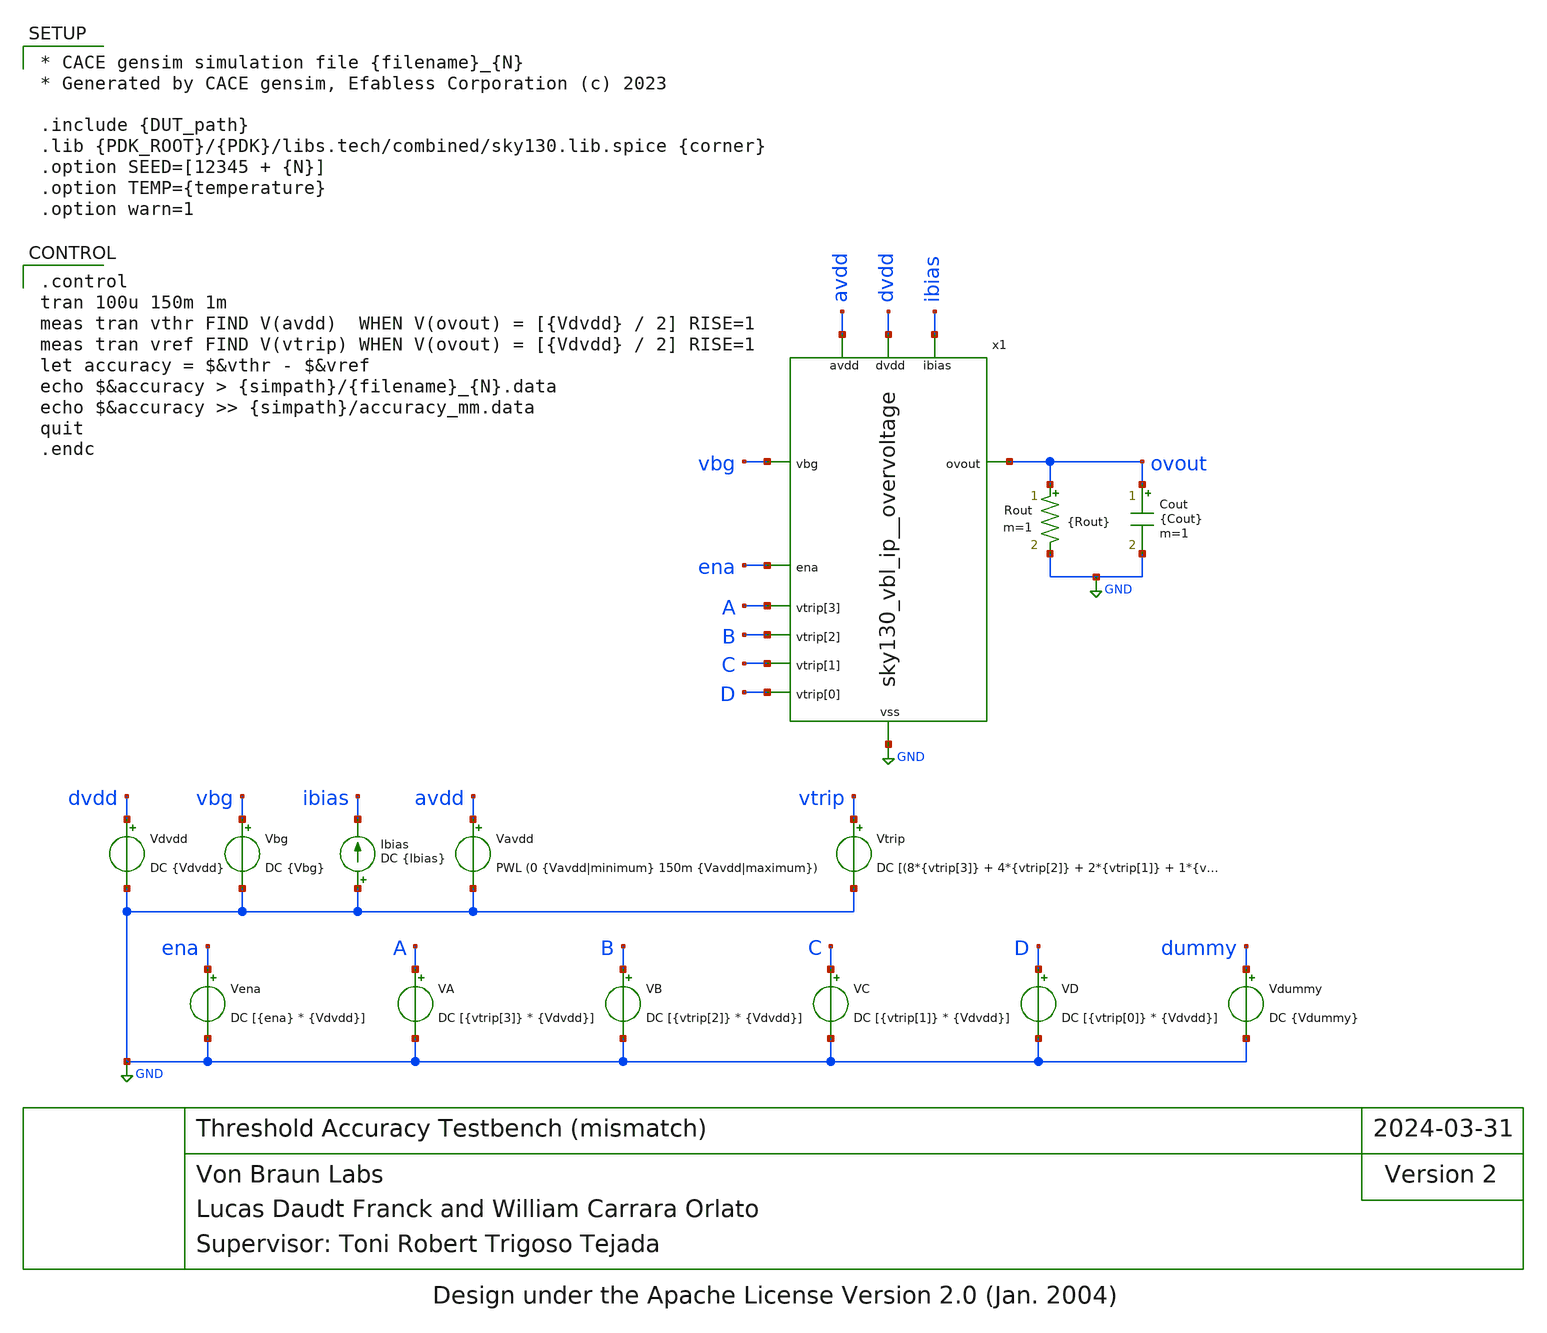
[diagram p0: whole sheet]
** sch_path: cace/tb_vacc_mm.sch
* Design under the Apache License Version 2.0 (Jan. 2004)
**.subckt tb_vacc_mm
Vavdd avdd GND PWL (0 {Vavdd|minimum} 150m {Vavdd|maximum})
Vdvdd dvdd GND DC {Vdvdd}
Vbg vbg GND DC {Vbg}
Ibias GND ibias DC {Ibias}
Vena ena GND DC [{ena} * {Vdvdd}]
VA A GND DC [{vtrip[3]} * {Vdvdd}]
VB B GND DC [{vtrip[2]} * {Vdvdd}]
VC C GND DC [{vtrip[1]} * {Vdvdd}]
VD D GND DC [{vtrip[0]} * {Vdvdd}]
Vtrip vtrip GND DC [(8*{vtrip[3]} + 4*{vtrip[2]} + 2*{vtrip[1]} + 1*{vtrip[0]})*0.14667 + 3.3]
Vdummy dummy GND DC {Vdummy}
Cout ovout GND {Cout} m=1
Rout ovout GND {Rout} m=1
x1 avdd dvdd ena A GND ibias B ovout vbg C D sky130_vbl_ip__overvoltage
**** begin user architecture code

* CACE gensim simulation file {filename}_{N}
* Generated by CACE gensim, Efabless Corporation (c) 2023

.include {DUT_path}
.lib {PDK_ROOT}/{PDK}/libs.tech/combined/sky130.lib.spice {corner}
.option SEED=[12345 + {N}]
.option TEMP={temperature}
.option warn=1



.control
tran 100u 150m 1m
meas tran vthr FIND V(avdd)  WHEN V(ovout) = [{Vdvdd} / 2] RISE=1
meas tran vref FIND V(vtrip) WHEN V(ovout) = [{Vdvdd} / 2] RISE=1
let accuracy = $&vthr - $&vref
echo $&accuracy > {simpath}/{filename}_{N}.data
echo $&accuracy >> {simpath}/accuracy_mm.data
quit
.endc


**** end user architecture code
**.ends
.GLOBAL GND
.end
